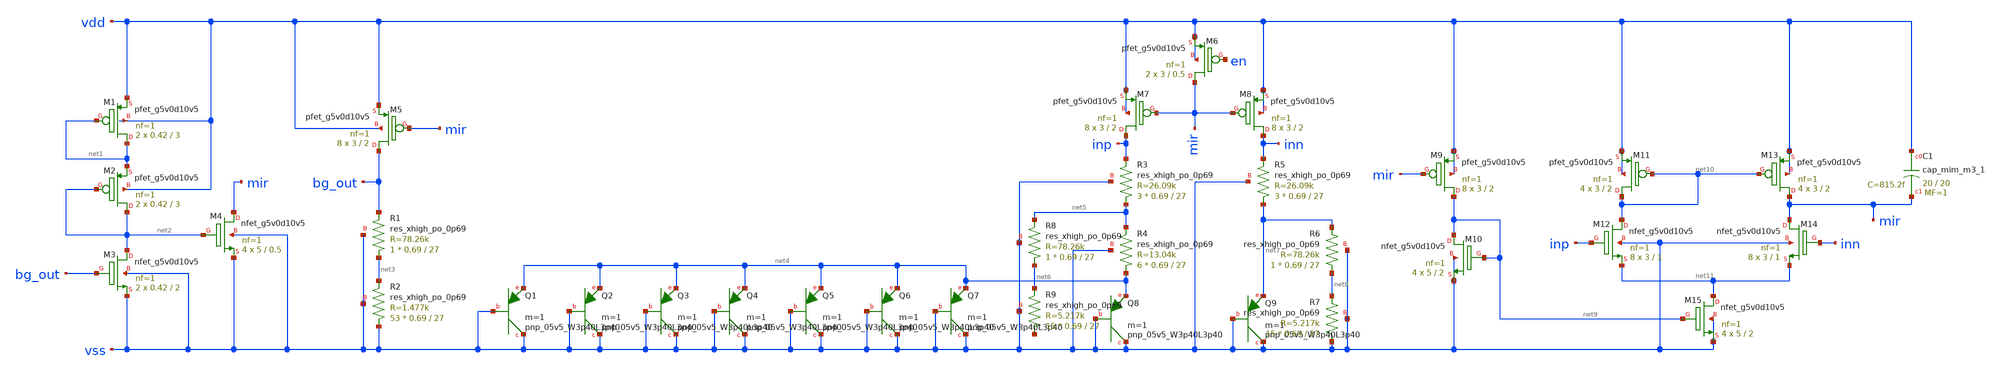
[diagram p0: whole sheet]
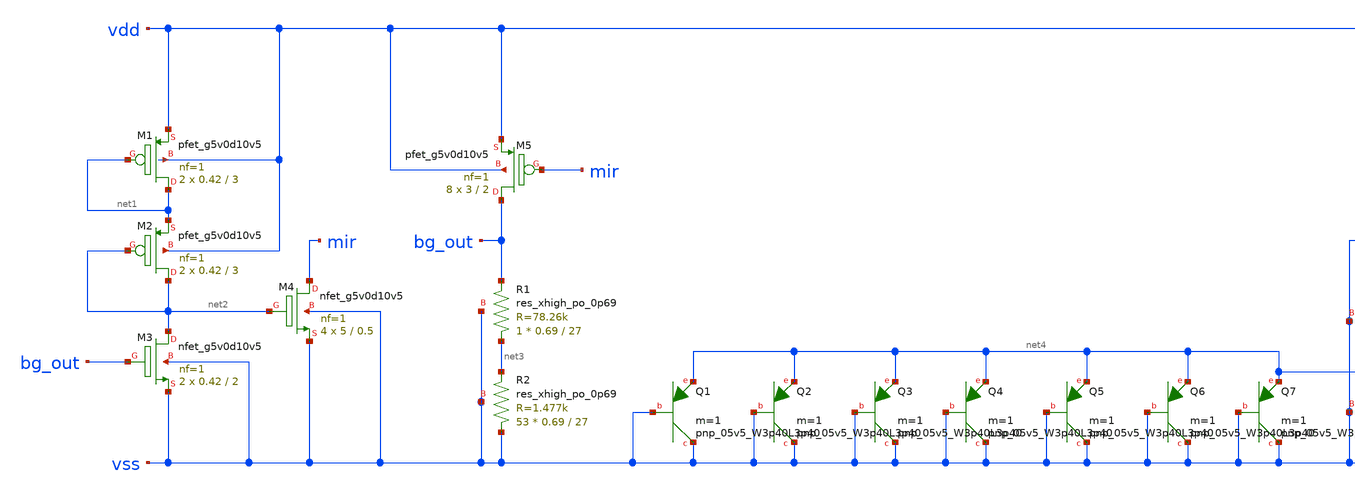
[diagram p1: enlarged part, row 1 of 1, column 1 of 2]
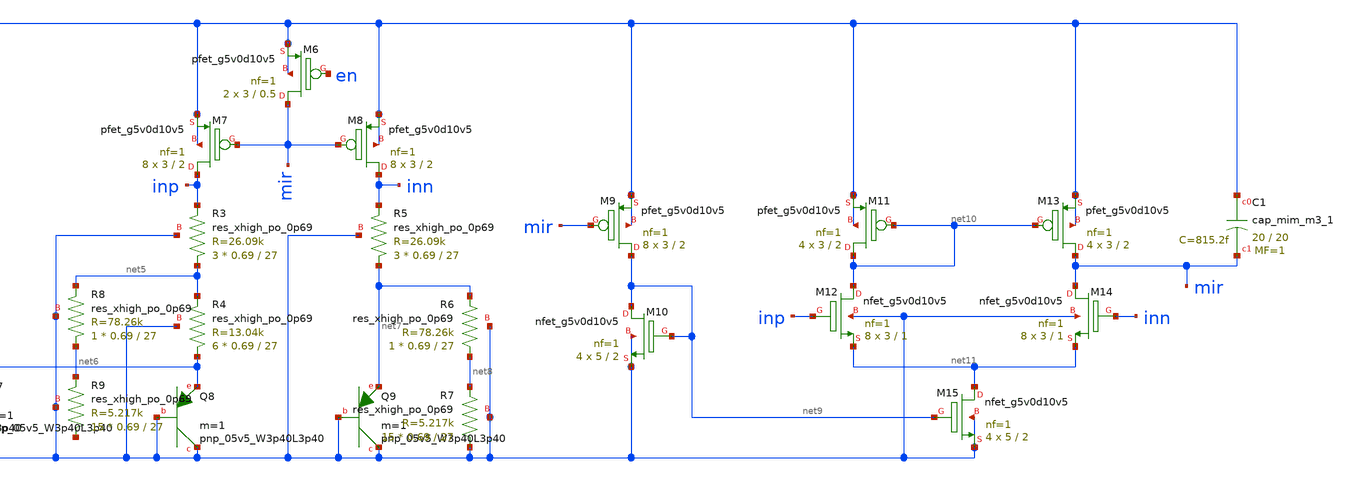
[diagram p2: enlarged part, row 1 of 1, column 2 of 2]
** sch_path: bandgap/untitled.sch
**.subckt untitled
XM1 net1 net1 vdd vdd sky130_fd_pr__pfet_g5v0d10v5 L=3 W=0.42 nf=1 ad='int((1 + 1)/2) * 0.42 / 1 * 0.29'
+ as='int((1 + 2)/2) * 0.42 / 1 * 0.29' pd='2*int((1 + 1)/2) * (0.42 / 1 + 0.29)' ps='2*int((1 + 2)/2) * (0.42 / 1 + 0.29)'
+ nrd='0.29 / 0.42 ' nrs='0.29 / 0.42 ' sa=0 sb=0 sd=0 mult=2 m=2
XM2 net2 net2 net1 vdd sky130_fd_pr__pfet_g5v0d10v5 L=3 W=0.42 nf=1 ad='int((1 + 1)/2) * 0.42 / 1 * 0.29'
+ as='int((1 + 2)/2) * 0.42 / 1 * 0.29' pd='2*int((1 + 1)/2) * (0.42 / 1 + 0.29)' ps='2*int((1 + 2)/2) * (0.42 / 1 + 0.29)'
+ nrd='0.29 / 0.42 ' nrs='0.29 / 0.42 ' sa=0 sb=0 sd=0 mult=2 m=2
XM3 net2 bg_out vss vss sky130_fd_pr__nfet_g5v0d10v5 L=2 W=0.42 nf=1 ad='int((1 + 1)/2) * 0.42 / 1 * 0.29'
+ as='int((1 + 2)/2) * 0.42 / 1 * 0.29' pd='2*int((1 + 1)/2) * (0.42 / 1 + 0.29)' ps='2*int((1 + 2)/2) * (0.42 / 1 + 0.29)'
+ nrd='0.29 / 0.42 ' nrs='0.29 / 0.42 ' sa=0 sb=0 sd=0 mult=2 m=2
XM4 mir net2 vss vss sky130_fd_pr__nfet_g5v0d10v5 L=0.5 W=5 nf=1 ad='int((1 + 1)/2) * 5 / 1 * 0.29' as='int((1 + 2)/2) * 5 / 1 * 0.29'
+ pd='2*int((1 + 1)/2) * (5 / 1 + 0.29)' ps='2*int((1 + 2)/2) * (5 / 1 + 0.29)' nrd='0.29 / 5 ' nrs='0.29 / 5 '
+ sa=0 sb=0 sd=0 mult=4 m=4
XM5 bg_out mir vdd vdd sky130_fd_pr__pfet_g5v0d10v5 L=2 W=3 nf=1 ad='int((1 + 1)/2) * 3 / 1 * 0.29' as='int((1 + 2)/2) * 3 / 1 * 0.29'
+ pd='2*int((1 + 1)/2) * (3 / 1 + 0.29)' ps='2*int((1 + 2)/2) * (3 / 1 + 0.29)' nrd='0.29 / 3 ' nrs='0.29 / 3 '
+ sa=0 sb=0 sd=0 mult=8 m=8
XR1 net3 bg_out vss sky130_fd_pr__res_xhigh_po_0p69 L=27 mult=1 m=1
XR2 vss net3 vss sky130_fd_pr__res_xhigh_po_0p69 L=27 mult=53 m=53
XQ1 vss vss net4 sky130_fd_pr__pnp_05v5_W3p40L3p40 m=1
XQ2 vss vss net4 sky130_fd_pr__pnp_05v5_W3p40L3p40 m=1
XQ3 vss vss net4 sky130_fd_pr__pnp_05v5_W3p40L3p40 m=1
XQ4 vss vss net4 sky130_fd_pr__pnp_05v5_W3p40L3p40 m=1
XQ5 vss vss net4 sky130_fd_pr__pnp_05v5_W3p40L3p40 m=1
XQ6 vss vss net4 sky130_fd_pr__pnp_05v5_W3p40L3p40 m=1
XQ7 vss vss net4 sky130_fd_pr__pnp_05v5_W3p40L3p40 m=1
XM6 mir en vdd vdd sky130_fd_pr__pfet_g5v0d10v5 L=0.5 W=3 nf=1 ad='int((1 + 1)/2) * 3 / 1 * 0.29' as='int((1 + 2)/2) * 3 / 1 * 0.29'
+ pd='2*int((1 + 1)/2) * (3 / 1 + 0.29)' ps='2*int((1 + 2)/2) * (3 / 1 + 0.29)' nrd='0.29 / 3 ' nrs='0.29 / 3 '
+ sa=0 sb=0 sd=0 mult=2 m=2
XM7 inp mir vdd vdd sky130_fd_pr__pfet_g5v0d10v5 L=2 W=3 nf=1 ad='int((1 + 1)/2) * 3 / 1 * 0.29' as='int((1 + 2)/2) * 3 / 1 * 0.29'
+ pd='2*int((1 + 1)/2) * (3 / 1 + 0.29)' ps='2*int((1 + 2)/2) * (3 / 1 + 0.29)' nrd='0.29 / 3 ' nrs='0.29 / 3 '
+ sa=0 sb=0 sd=0 mult=8 m=8
XM8 inn mir vdd vdd sky130_fd_pr__pfet_g5v0d10v5 L=2 W=3 nf=1 ad='int((1 + 1)/2) * 3 / 1 * 0.29' as='int((1 + 2)/2) * 3 / 1 * 0.29'
+ pd='2*int((1 + 1)/2) * (3 / 1 + 0.29)' ps='2*int((1 + 2)/2) * (3 / 1 + 0.29)' nrd='0.29 / 3 ' nrs='0.29 / 3 '
+ sa=0 sb=0 sd=0 mult=8 m=8
XR3 net5 inp vss sky130_fd_pr__res_xhigh_po_0p69 L=27 mult=3 m=3
XR4 net4 net5 vss sky130_fd_pr__res_xhigh_po_0p69 L=27 mult=6 m=6
XQ8 vss vss net4 sky130_fd_pr__pnp_05v5_W3p40L3p40 m=1
XR5 net7 inn vss sky130_fd_pr__res_xhigh_po_0p69 L=27 mult=3 m=3
XQ9 vss vss net7 sky130_fd_pr__pnp_05v5_W3p40L3p40 m=1
XR6 net8 net7 vss sky130_fd_pr__res_xhigh_po_0p69 L=27 mult=1 m=1
XR7 vss net8 vss sky130_fd_pr__res_xhigh_po_0p69 L=27 mult=15 m=15
XR8 net6 net5 vss sky130_fd_pr__res_xhigh_po_0p69 L=27 mult=1 m=1
XR9 net12 net6 vss sky130_fd_pr__res_xhigh_po_0p69 L=27 mult=15 m=15
XM9 net9 mir vdd vdd sky130_fd_pr__pfet_g5v0d10v5 L=2 W=3 nf=1 ad='int((1 + 1)/2) * 3 / 1 * 0.29' as='int((1 + 2)/2) * 3 / 1 * 0.29'
+ pd='2*int((1 + 1)/2) * (3 / 1 + 0.29)' ps='2*int((1 + 2)/2) * (3 / 1 + 0.29)' nrd='0.29 / 3 ' nrs='0.29 / 3 '
+ sa=0 sb=0 sd=0 mult=8 m=8
XM10 net9 net9 vss vss sky130_fd_pr__nfet_g5v0d10v5 L=2 W=5 nf=1 ad='int((1 + 1)/2) * 5 / 1 * 0.29' as='int((1 + 2)/2) * 5 / 1 * 0.29'
+ pd='2*int((1 + 1)/2) * (5 / 1 + 0.29)' ps='2*int((1 + 2)/2) * (5 / 1 + 0.29)' nrd='0.29 / 5 ' nrs='0.29 / 5 '
+ sa=0 sb=0 sd=0 mult=4 m=4
XM11 net10 net10 vdd vdd sky130_fd_pr__pfet_g5v0d10v5 L=2 W=3 nf=1 ad='int((1 + 1)/2) * 3 / 1 * 0.29'
+ as='int((1 + 2)/2) * 3 / 1 * 0.29' pd='2*int((1 + 1)/2) * (3 / 1 + 0.29)' ps='2*int((1 + 2)/2) * (3 / 1 + 0.29)'
+ nrd='0.29 / 3 ' nrs='0.29 / 3 ' sa=0 sb=0 sd=0 mult=4 m=4
XM12 net10 inp net11 vss sky130_fd_pr__nfet_g5v0d10v5 L=1 W=3 nf=1 ad='int((1 + 1)/2) * 3 / 1 * 0.29'
+ as='int((1 + 2)/2) * 3 / 1 * 0.29' pd='2*int((1 + 1)/2) * (3 / 1 + 0.29)' ps='2*int((1 + 2)/2) * (3 / 1 + 0.29)'
+ nrd='0.29 / 3 ' nrs='0.29 / 3 ' sa=0 sb=0 sd=0 mult=8 m=8
XM13 mir net10 vdd vdd sky130_fd_pr__pfet_g5v0d10v5 L=2 W=3 nf=1 ad='int((1 + 1)/2) * 3 / 1 * 0.29' as='int((1 + 2)/2) * 3 / 1 * 0.29'
+ pd='2*int((1 + 1)/2) * (3 / 1 + 0.29)' ps='2*int((1 + 2)/2) * (3 / 1 + 0.29)' nrd='0.29 / 3 ' nrs='0.29 / 3 '
+ sa=0 sb=0 sd=0 mult=4 m=4
XM14 mir inn net11 vss sky130_fd_pr__nfet_g5v0d10v5 L=1 W=3 nf=1 ad='int((1 + 1)/2) * 3 / 1 * 0.29' as='int((1 + 2)/2) * 3 / 1 * 0.29'
+ pd='2*int((1 + 1)/2) * (3 / 1 + 0.29)' ps='2*int((1 + 2)/2) * (3 / 1 + 0.29)' nrd='0.29 / 3 ' nrs='0.29 / 3 '
+ sa=0 sb=0 sd=0 mult=8 m=8
XM15 net11 net9 vss vss sky130_fd_pr__nfet_g5v0d10v5 L=2 W=5 nf=1 ad='int((1 + 1)/2) * 5 / 1 * 0.29'
+ as='int((1 + 2)/2) * 5 / 1 * 0.29' pd='2*int((1 + 1)/2) * (5 / 1 + 0.29)' ps='2*int((1 + 2)/2) * (5 / 1 + 0.29)'
+ nrd='0.29 / 5 ' nrs='0.29 / 5 ' sa=0 sb=0 sd=0 mult=4 m=4
XC1 vdd mir sky130_fd_pr__cap_mim_m3_1 W=20 L=20 MF=1 m=1
**.ends
.end
